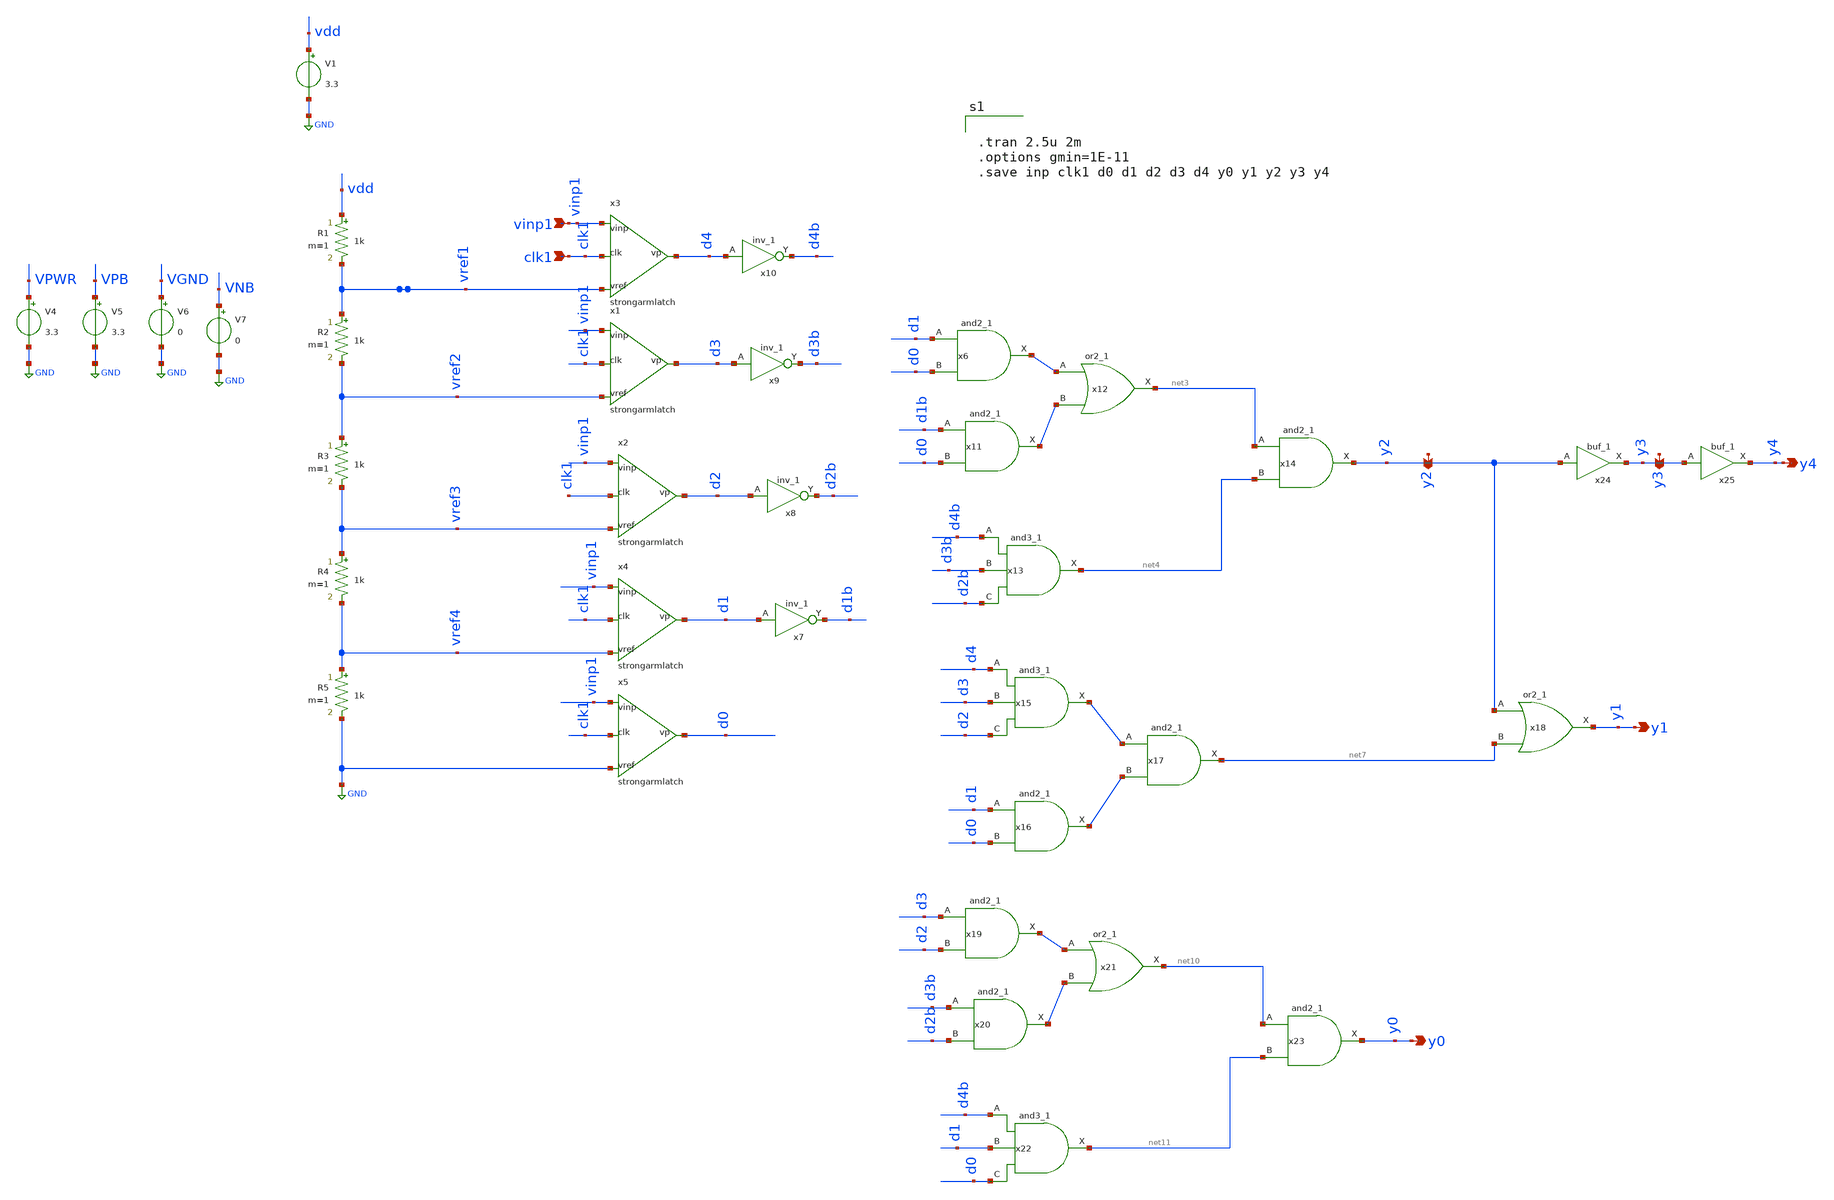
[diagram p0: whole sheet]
** sch_path: xschem/FDC/adc1.sch
**.subckt adc1 vinp1 clk1 y1 y4 y0 y3 y2
*.ipin vinp1
*.ipin clk1
*.opin y1
*.opin y4
*.opin y0
*.opin y3
*.opin y2
V1 vdd GND 3.3
x3 vinp1 vref1 d4 clk1 strongarmlatch
R1 vdd vref1 1k m=1
R2 vref1 vref2 1k m=1
R3 vref2 vref3 1k m=1
R4 vref3 vref4 1k m=1
R5 vref4 GND 1k m=1
x1 vinp1 vref2 d3 clk1 strongarmlatch
x2 vinp1 vref3 d2 clk1 strongarmlatch
x4 vinp1 vref4 d1 clk1 strongarmlatch
x5 vinp1 GND d0 clk1 strongarmlatch
x7 d1 VGND VNB VPB VPWR d1b sky130_fd_sc_hvl__inv_1
x8 d2 VGND VNB VPB VPWR d2b sky130_fd_sc_hvl__inv_1
x9 d3 VGND VNB VPB VPWR d3b sky130_fd_sc_hvl__inv_1
x10 d4 VGND VNB VPB VPWR d4b sky130_fd_sc_hvl__inv_1
V4 VPWR GND 3.3
V5 VPB GND 3.3
V6 VGND GND 0
V7 VNB GND 0
x6 d1 d0 VGND VNB VPB VPWR net1 sky130_fd_sc_hvl__and2_1
x11 d1b d0 VGND VNB VPB VPWR net2 sky130_fd_sc_hvl__and2_1
x12 net1 net2 VGND VNB VPB VPWR net3 sky130_fd_sc_hvl__or2_1
x13 d4b d3b d2b VGND VNB VPB VPWR net4 sky130_fd_sc_hvl__and3_1
x14 net3 net4 VGND VNB VPB VPWR y2 sky130_fd_sc_hvl__and2_1
x15 d4 d3 d2 VGND VNB VPB VPWR net5 sky130_fd_sc_hvl__and3_1
x16 d1 d0 VGND VNB VPB VPWR net6 sky130_fd_sc_hvl__and2_1
x17 net5 net6 VGND VNB VPB VPWR net7 sky130_fd_sc_hvl__and2_1
x18 y2 net7 VGND VNB VPB VPWR y1 sky130_fd_sc_hvl__or2_1
x19 d3 d2 VGND VNB VPB VPWR net8 sky130_fd_sc_hvl__and2_1
x20 d3b d2b VGND VNB VPB VPWR net9 sky130_fd_sc_hvl__and2_1
x21 net8 net9 VGND VNB VPB VPWR net10 sky130_fd_sc_hvl__or2_1
x22 d4b d1 d0 VGND VNB VPB VPWR net11 sky130_fd_sc_hvl__and3_1
x23 net10 net11 VGND VNB VPB VPWR y0 sky130_fd_sc_hvl__and2_1
x24 y2 VGND VNB VPB VPWR y3 sky130_fd_sc_hvl__buf_1
x25 y3 VGND VNB VPB VPWR y4 sky130_fd_sc_hvl__buf_1
**** begin user architecture code

.lib ~/open_pdks/sky130/sky130A/libs.tech/ngspice/sky130.lib.spice tt
.include /home/vinodhini/open_pdks/sky130/sky130A/libs.ref/sky130_fd_sc_hvl/spice/sky130_fd_sc_hvl.spice

*.MODEL swmod SW(VT=0.0 VH=0.01 RON=1 ROFF=10000000000)
.param mc_mm_switch=0
.param mc_pr_switch=0


.tran 2.5u 2m
.options gmin=1E-11
.save inp clk1 d0 d1 d2 d3 d4 y0 y1 y2 y3 y4

**** end user architecture code
**.ends

* expanding   symbol:  /home/vinodhini/Documents/strongarmlatch.sym # of pins=4
** sym_path: xschem/FDC/strongarmlatch.sym
** sch_path: xschem/FDC/strongarmlatch.sch
.subckt strongarmlatch vinp vref vp clk
*.ipin vinp
*.ipin vref
*.ipin clk
*.opin vp
XM7 net5 vinp net3 GND sky130_fd_pr__nfet_g5v0d10v5 L=0.5 W=12 nf=1 ad='int((nf+1)/2) * W/nf * 0.29'
+ as='int((nf+2)/2) * W/nf * 0.29' pd='2*int((nf+1)/2) * (W/nf + 0.29)' ps='2*int((nf+2)/2) * (W/nf + 0.29)'
+ nrd='0.29 / W' nrs='0.29 / W' sa=0 sb=0 sd=0 mult=1 m=1
XM8 net4 vref net3 GND sky130_fd_pr__nfet_g5v0d10v5 L=0.5 W=12 nf=1 ad='int((nf+1)/2) * W/nf * 0.29'
+ as='int((nf+2)/2) * W/nf * 0.29' pd='2*int((nf+1)/2) * (W/nf + 0.29)' ps='2*int((nf+2)/2) * (W/nf + 0.29)'
+ nrd='0.29 / W' nrs='0.29 / W' sa=0 sb=0 sd=0 mult=1 m=1
XM3 net2 net1 vdda vdda sky130_fd_pr__pfet_g5v0d10v5 L=0.5 W=8 nf=1 ad='int((nf+1)/2) * W/nf * 0.29'
+ as='int((nf+2)/2) * W/nf * 0.29' pd='2*int((nf+1)/2) * (W/nf + 0.29)' ps='2*int((nf+2)/2) * (W/nf + 0.29)'
+ nrd='0.29 / W' nrs='0.29 / W' sa=0 sb=0 sd=0 mult=1 m=1
XM9 net2 clk vdda vdda sky130_fd_pr__pfet_g5v0d10v5 L=0.5 W=8 nf=1 ad='int((nf+1)/2) * W/nf * 0.29' as='int((nf+2)/2) * W/nf * 0.29'
+ pd='2*int((nf+1)/2) * (W/nf + 0.29)' ps='2*int((nf+2)/2) * (W/nf + 0.29)' nrd='0.29 / W' nrs='0.29 / W'
+ sa=0 sb=0 sd=0 mult=1 m=1
XM4 net1 clk vdda vdda sky130_fd_pr__pfet_g5v0d10v5 L=0.5 W=8 nf=1 ad='int((nf+1)/2) * W/nf * 0.29' as='int((nf+2)/2) * W/nf * 0.29'
+ pd='2*int((nf+1)/2) * (W/nf + 0.29)' ps='2*int((nf+2)/2) * (W/nf + 0.29)' nrd='0.29 / W' nrs='0.29 / W'
+ sa=0 sb=0 sd=0 mult=1 m=1
XM10 net1 net2 vdda vdda sky130_fd_pr__pfet_g5v0d10v5 L=0.5 W=8 nf=1 ad='int((nf+1)/2) * W/nf * 0.29'
+ as='int((nf+2)/2) * W/nf * 0.29' pd='2*int((nf+1)/2) * (W/nf + 0.29)' ps='2*int((nf+2)/2) * (W/nf + 0.29)'
+ nrd='0.29 / W' nrs='0.29 / W' sa=0 sb=0 sd=0 mult=1 m=1
XM11 net4 clk vdda vdda sky130_fd_pr__pfet_g5v0d10v5 L=0.5 W=8 nf=1 ad='int((nf+1)/2) * W/nf * 0.29'
+ as='int((nf+2)/2) * W/nf * 0.29' pd='2*int((nf+1)/2) * (W/nf + 0.29)' ps='2*int((nf+2)/2) * (W/nf + 0.29)'
+ nrd='0.29 / W' nrs='0.29 / W' sa=0 sb=0 sd=0 mult=1 m=1
XM12 net5 clk vdda vdda sky130_fd_pr__pfet_g5v0d10v5 L=0.5 W=8 nf=1 ad='int((nf+1)/2) * W/nf * 0.29'
+ as='int((nf+2)/2) * W/nf * 0.29' pd='2*int((nf+1)/2) * (W/nf + 0.29)' ps='2*int((nf+2)/2) * (W/nf + 0.29)'
+ nrd='0.29 / W' nrs='0.29 / W' sa=0 sb=0 sd=0 mult=1 m=1
XM13 net3 clk vssa vssa sky130_fd_pr__nfet_g5v0d10v5 L=0.5 W=8 nf=1 ad='int((nf+1)/2) * W/nf * 0.29'
+ as='int((nf+2)/2) * W/nf * 0.29' pd='2*int((nf+1)/2) * (W/nf + 0.29)' ps='2*int((nf+2)/2) * (W/nf + 0.29)'
+ nrd='0.29 / W' nrs='0.29 / W' sa=0 sb=0 sd=0 mult=1 m=1
XM14 net3 vinp net4 vdda sky130_fd_pr__pfet_g5v0d10v5 L=0.5 W=8 nf=1 ad='int((nf+1)/2) * W/nf * 0.29'
+ as='int((nf+2)/2) * W/nf * 0.29' pd='2*int((nf+1)/2) * (W/nf + 0.29)' ps='2*int((nf+2)/2) * (W/nf + 0.29)'
+ nrd='0.29 / W' nrs='0.29 / W' sa=0 sb=0 sd=0 mult=1 m=1
XM15 net3 vref net5 vdda sky130_fd_pr__pfet_g5v0d10v5 L=0.5 W=8 nf=1 ad='int((nf+1)/2) * W/nf * 0.29'
+ as='int((nf+2)/2) * W/nf * 0.29' pd='2*int((nf+1)/2) * (W/nf + 0.29)' ps='2*int((nf+2)/2) * (W/nf + 0.29)'
+ nrd='0.29 / W' nrs='0.29 / W' sa=0 sb=0 sd=0 mult=1 m=1
XM16 vm vop GND GND sky130_fd_pr__nfet_g5v0d10v5 L=0.5 W=1 nf=1 ad='int((nf+1)/2) * W/nf * 0.29' as='int((nf+2)/2) * W/nf * 0.29'
+ pd='2*int((nf+1)/2) * (W/nf + 0.29)' ps='2*int((nf+2)/2) * (W/nf + 0.29)' nrd='0.29 / W' nrs='0.29 / W'
+ sa=0 sb=0 sd=0 mult=1 m=1
XM17 vp vom GND GND sky130_fd_pr__nfet_g5v0d10v5 L=0.5 W=1 nf=1 ad='int((nf+1)/2) * W/nf * 0.29' as='int((nf+2)/2) * W/nf * 0.29'
+ pd='2*int((nf+1)/2) * (W/nf + 0.29)' ps='2*int((nf+2)/2) * (W/nf + 0.29)' nrd='0.29 / W' nrs='0.29 / W'
+ sa=0 sb=0 sd=0 mult=1 m=1
XM1 net2 net1 net5 GND sky130_fd_pr__nfet_g5v0d10v5 L=0.5 W=4 nf=1 ad='int((nf+1)/2) * W/nf * 0.29' as='int((nf+2)/2) * W/nf * 0.29'
+ pd='2*int((nf+1)/2) * (W/nf + 0.29)' ps='2*int((nf+2)/2) * (W/nf + 0.29)' nrd='0.29 / W' nrs='0.29 / W'
+ sa=0 sb=0 sd=0 mult=1 m=1
XM2 net1 net2 net4 GND sky130_fd_pr__nfet_g5v0d10v5 L=0.5 W=4 nf=1 ad='int((nf+1)/2) * W/nf * 0.29' as='int((nf+2)/2) * W/nf * 0.29'
+ pd='2*int((nf+1)/2) * (W/nf + 0.29)' ps='2*int((nf+2)/2) * (W/nf + 0.29)' nrd='0.29 / W' nrs='0.29 / W'
+ sa=0 sb=0 sd=0 mult=1 m=1
x1 net1 VGND VNB VPB VPWR vom sky130_fd_sc_hvl__inv_1
x2 net2 VGND VNB VPB VPWR vop sky130_fd_sc_hvl__inv_1
x4 vm VGND VNB VPB VPWR vp sky130_fd_sc_hvl__inv_1
x3 vp VGND VNB VPB VPWR vm sky130_fd_sc_hvl__inv_1
V1 vdda vssa 3.3
V2 vssa GND 0
V3 VPWR vssa 3.3
V4 VPB vssa 3.3
V5 VGND vssa 0
V6 VNB vssa 0
.ends

.GLOBAL GND
.end
